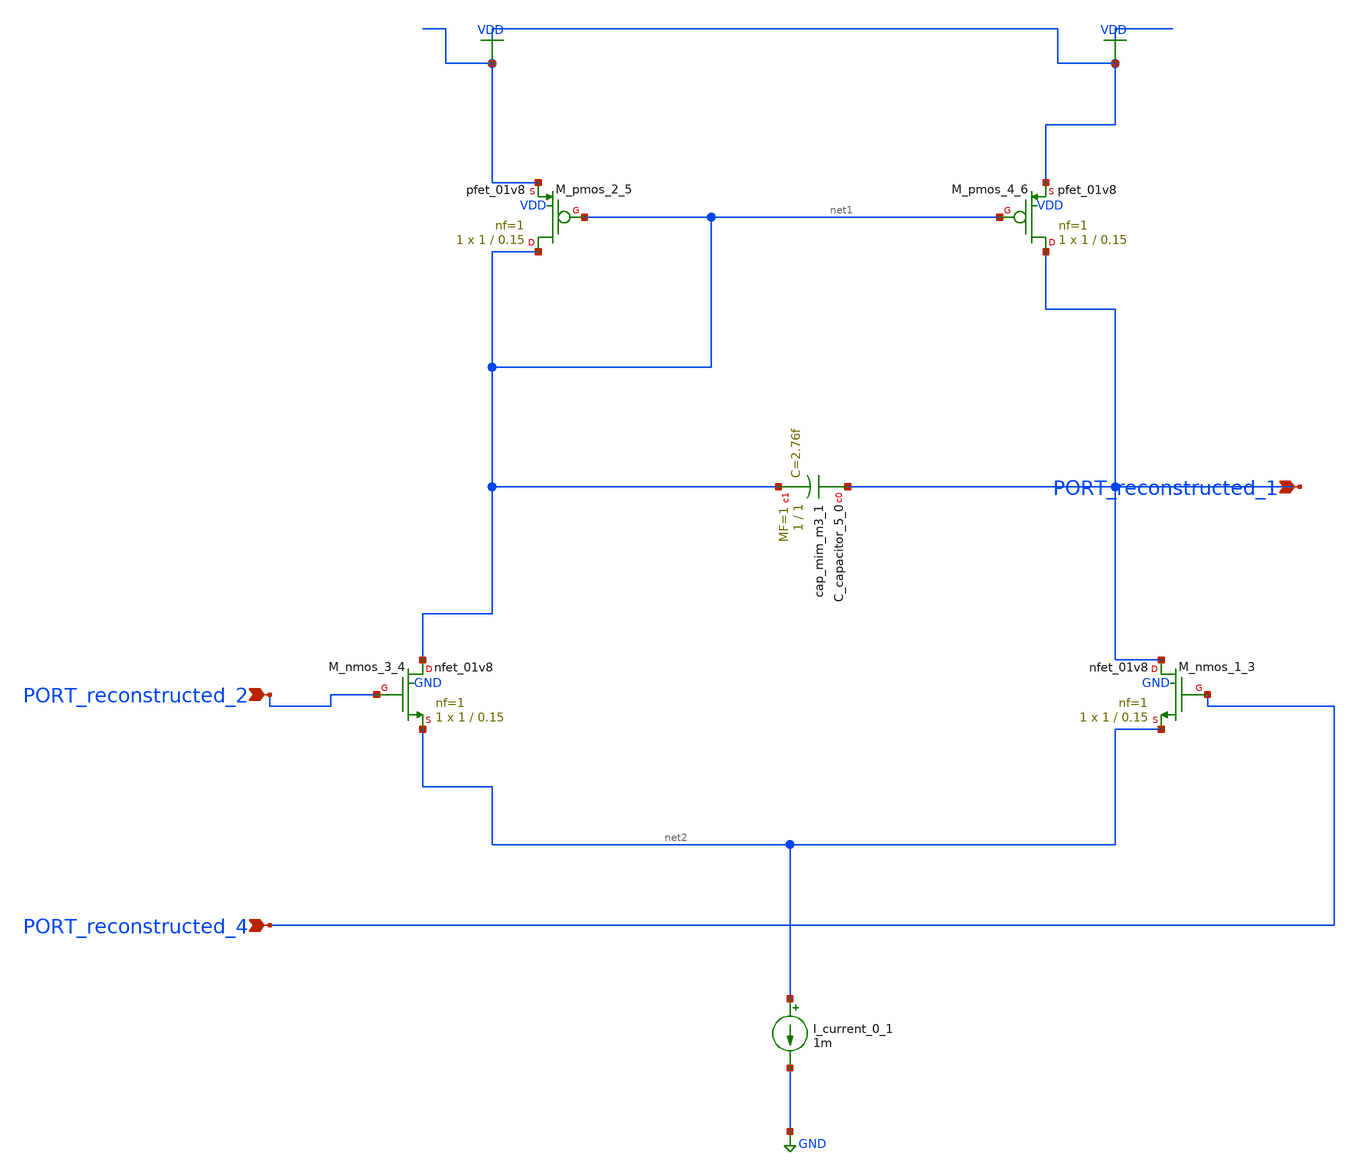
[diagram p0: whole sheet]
** sch_path: schematics/AMSNet/421.sch
**.subckt 421 PORT_reconstructed_1 PORT_reconstructed_2 PORT_reconstructed_4
*.ipin PORT_reconstructed_1
*.ipin PORT_reconstructed_2
*.ipin PORT_reconstructed_4
XC_capacitor_5_0 PORT_reconstructed_1 net1 sky130_fd_pr__cap_mim_m3_1 W=1 L=1 MF=1 m=1
I_current_0_1 net2 GND 1m
XM_nmos_1_3 PORT_reconstructed_1 PORT_reconstructed_4 net2 GND sky130_fd_pr__nfet_01v8 L=0.15 W=1 nf=1
+ ad='int((1 + 1)/2) * 1 / 1 * 0.29' as='int((1 + 2)/2) * 1 / 1 * 0.29' pd='2*int((1 + 1)/2) * (1 / 1 + 0.29)'
+ ps='2*int((1 + 2)/2) * (1 / 1 + 0.29)' nrd='0.29 / 1 ' nrs='0.29 / 1 ' sa=0 sb=0 sd=0 mult=1 m=1
XM_nmos_3_4 net1 PORT_reconstructed_2 net2 GND sky130_fd_pr__nfet_01v8 L=0.15 W=1 nf=1 ad='int((1 + 1)/2) * 1 / 1 * 0.29'
+ as='int((1 + 2)/2) * 1 / 1 * 0.29' pd='2*int((1 + 1)/2) * (1 / 1 + 0.29)' ps='2*int((1 + 2)/2) * (1 / 1 + 0.29)'
+ nrd='0.29 / 1 ' nrs='0.29 / 1 ' sa=0 sb=0 sd=0 mult=1 m=1
XM_pmos_2_5 net1 net1 VDD VDD sky130_fd_pr__pfet_01v8 L=0.15 W=1 nf=1 ad='int((1 + 1)/2) * 1 / 1 * 0.29'
+ as='int((1 + 2)/2) * 1 / 1 * 0.29' pd='2*int((1 + 1)/2) * (1 / 1 + 0.29)' ps='2*int((1 + 2)/2) * (1 / 1 + 0.29)'
+ nrd='0.29 / 1 ' nrs='0.29 / 1 ' sa=0 sb=0 sd=0 mult=1 m=1
XM_pmos_4_6 PORT_reconstructed_1 net1 VDD VDD sky130_fd_pr__pfet_01v8 L=0.15 W=1 nf=1 ad='int((1 + 1)/2) * 1 / 1 * 0.29'
+ as='int((1 + 2)/2) * 1 / 1 * 0.29' pd='2*int((1 + 1)/2) * (1 / 1 + 0.29)' ps='2*int((1 + 2)/2) * (1 / 1 + 0.29)'
+ nrd='0.29 / 1 ' nrs='0.29 / 1 ' sa=0 sb=0 sd=0 mult=1 m=1
**.ends
.GLOBAL GND
.GLOBAL VDD
.end
